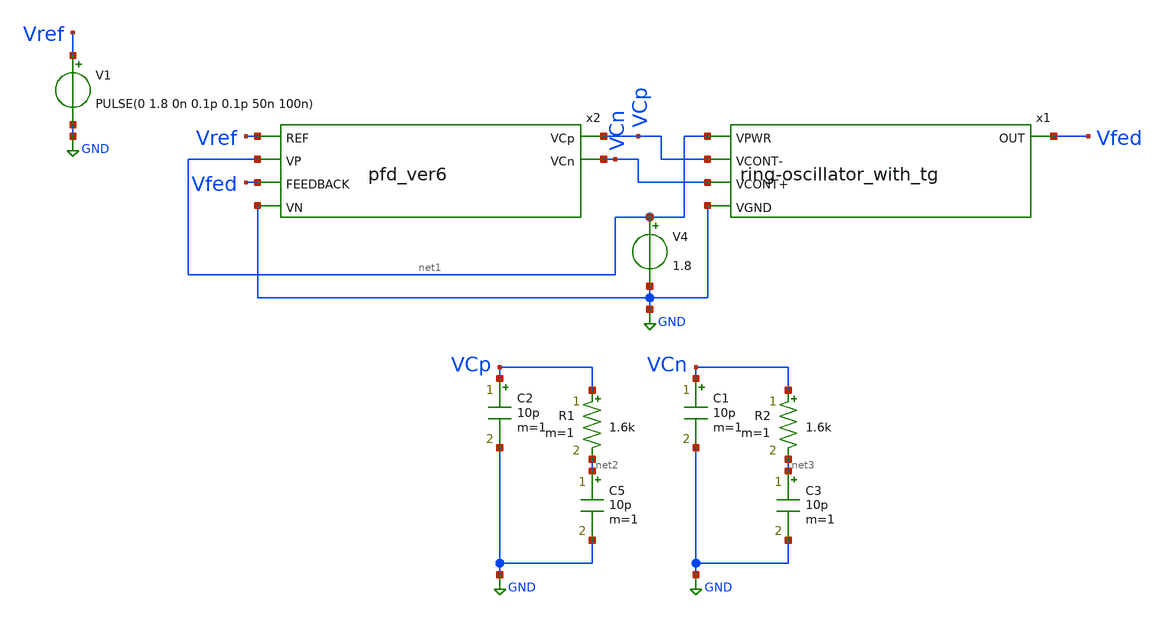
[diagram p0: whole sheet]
** sch_path: xschem_sch/pll_tb.sch
**.subckt pll_tb
V1 Vref GND PULSE(0 1.8 0n 0.1p 0.1p 50n 100n)
x1 net1 VCp Vfed VCn GND ring-oscillator_with_tg
V4 net1 GND 1.8
x2 Vref VCp VCn net1 Vfed GND pfd_ver6
C2 VCp GND 10p m=1
C5 net2 GND 10p m=1
R1 VCp net2 1.6k m=1
C1 VCn GND 10p m=1
C3 net3 GND 10p m=1
R2 VCn net3 1.6k m=1
**** begin user architecture code


.option wnflag=1
.option savecurrents
.control
save all
tran 1n 50u 0
plot VCp VCn
plot Vref Vfed
plot Vfed
.endc



** opencircuitdesign pdks install
.lib $::SKYWATER_MODELS/sky130.lib.spice tt
.param mc_mmm_cwitch=0
.param mc_pr_switch=1

**** end user architecture code
**.ends

* expanding   symbol:  ring-oscillator_with_tg.sym # of pins=5
** sym_path: xschem_sch/ring-oscillator_with_tg.sym
** sch_path: xschem_sch/ring-oscillator_with_tg.sch
.subckt ring-oscillator_with_tg VPWR VCONT- OUT VCONT+ VGND
*.ipin VPWR
*.opin OUT
*.ipin VGND
*.ipin VCONT+
*.ipin VCONT-
XM7 net1 net5 VPWR VPWR sky130_fd_pr__pfet_01v8 L=0.2 W=0.45 nf=1 ad='int((nf+1)/2) * W/nf * 0.29' as='int((nf+2)/2) * W/nf * 0.29'
+ pd='2*int((nf+1)/2) * (W/nf + 0.29)' ps='2*int((nf+2)/2) * (W/nf + 0.29)' nrd='0.29 / W' nrs='0.29 / W'
+ sa=0 sb=0 sd=0 mult=1 m=1
XM8 net3 VCONT- net1 VPWR sky130_fd_pr__pfet_01v8 L=0.2 W=0.45 nf=1 ad='int((nf+1)/2) * W/nf * 0.29'
+ as='int((nf+2)/2) * W/nf * 0.29' pd='2*int((nf+1)/2) * (W/nf + 0.29)' ps='2*int((nf+2)/2) * (W/nf + 0.29)'
+ nrd='0.29 / W' nrs='0.29 / W' sa=0 sb=0 sd=0 mult=1 m=1
XM9 net2 net3 VPWR VPWR sky130_fd_pr__pfet_01v8 L=0.2 W=0.45 nf=1 ad='int((nf+1)/2) * W/nf * 0.29' as='int((nf+2)/2) * W/nf * 0.29'
+ pd='2*int((nf+1)/2) * (W/nf + 0.29)' ps='2*int((nf+2)/2) * (W/nf + 0.29)' nrd='0.29 / W' nrs='0.29 / W'
+ sa=0 sb=0 sd=0 mult=1 m=1
XM11 OUT net4 VPWR VPWR sky130_fd_pr__pfet_01v8 L=0.2 W=0.45 nf=1 ad='int((nf+1)/2) * W/nf * 0.29' as='int((nf+2)/2) * W/nf * 0.29'
+ pd='2*int((nf+1)/2) * (W/nf + 0.29)' ps='2*int((nf+2)/2) * (W/nf + 0.29)' nrd='0.29 / W' nrs='0.29 / W'
+ sa=0 sb=0 sd=0 mult=1 m=1
XM10 net4 VCONT- net2 VPWR sky130_fd_pr__pfet_01v8 L=0.2 W=0.45 nf=1 ad='int((nf+1)/2) * W/nf * 0.29'
+ as='int((nf+2)/2) * W/nf * 0.29' pd='2*int((nf+1)/2) * (W/nf + 0.29)' ps='2*int((nf+2)/2) * (W/nf + 0.29)'
+ nrd='0.29 / W' nrs='0.29 / W' sa=0 sb=0 sd=0 mult=1 m=1
XM12 net5 VCONT- OUT VPWR sky130_fd_pr__pfet_01v8 L=0.2 W=0.45 nf=1 ad='int((nf+1)/2) * W/nf * 0.29'
+ as='int((nf+2)/2) * W/nf * 0.29' pd='2*int((nf+1)/2) * (W/nf + 0.29)' ps='2*int((nf+2)/2) * (W/nf + 0.29)'
+ nrd='0.29 / W' nrs='0.29 / W' sa=0 sb=0 sd=0 mult=1 m=1
XC1 VGND net5 sky130_fd_pr__cap_mim_m3_1 W=10 L=10 MF=1 m=1
XC2 VGND net3 sky130_fd_pr__cap_mim_m3_1 W=10 L=10 MF=1 m=1
XC3 VGND net4 sky130_fd_pr__cap_mim_m3_1 W=10 L=10 MF=10 m=10
XM13 OUT net4 VGND VGND sky130_fd_pr__nfet_01v8 L=0.2 W=0.45 nf=1 ad='int((nf+1)/2) * W/nf * 0.29' as='int((nf+2)/2) * W/nf * 0.29'
+ pd='2*int((nf+1)/2) * (W/nf + 0.29)' ps='2*int((nf+2)/2) * (W/nf + 0.29)' nrd='0.29 / W' nrs='0.29 / W'
+ sa=0 sb=0 sd=0 mult=1 m=1
XM1 net2 net3 VGND VGND sky130_fd_pr__nfet_01v8 L=0.2 W=0.45 nf=1 ad='int((nf+1)/2) * W/nf * 0.29' as='int((nf+2)/2) * W/nf * 0.29'
+ pd='2*int((nf+1)/2) * (W/nf + 0.29)' ps='2*int((nf+2)/2) * (W/nf + 0.29)' nrd='0.29 / W' nrs='0.29 / W'
+ sa=0 sb=0 sd=0 mult=1 m=1
XM2 net1 net5 VGND VGND sky130_fd_pr__nfet_01v8 L=0.2 W=0.45 nf=1 ad='int((nf+1)/2) * W/nf * 0.29' as='int((nf+2)/2) * W/nf * 0.29'
+ pd='2*int((nf+1)/2) * (W/nf + 0.29)' ps='2*int((nf+2)/2) * (W/nf + 0.29)' nrd='0.29 / W' nrs='0.29 / W'
+ sa=0 sb=0 sd=0 mult=1 m=1
XM3 OUT VCONT+ net5 VGND sky130_fd_pr__nfet_01v8 L=0.2 W=0.45 nf=1 ad='int((nf+1)/2) * W/nf * 0.29' as='int((nf+2)/2) * W/nf * 0.29'
+ pd='2*int((nf+1)/2) * (W/nf + 0.29)' ps='2*int((nf+2)/2) * (W/nf + 0.29)' nrd='0.29 / W' nrs='0.29 / W'
+ sa=0 sb=0 sd=0 mult=1 m=1
XM4 net1 VCONT+ net3 VGND sky130_fd_pr__nfet_01v8 L=0.2 W=0.45 nf=1 ad='int((nf+1)/2) * W/nf * 0.29'
+ as='int((nf+2)/2) * W/nf * 0.29' pd='2*int((nf+1)/2) * (W/nf + 0.29)' ps='2*int((nf+2)/2) * (W/nf + 0.29)'
+ nrd='0.29 / W' nrs='0.29 / W' sa=0 sb=0 sd=0 mult=1 m=1
XM5 net2 VCONT+ net4 VGND sky130_fd_pr__nfet_01v8 L=0.2 W=0.45 nf=1 ad='int((nf+1)/2) * W/nf * 0.29'
+ as='int((nf+2)/2) * W/nf * 0.29' pd='2*int((nf+1)/2) * (W/nf + 0.29)' ps='2*int((nf+2)/2) * (W/nf + 0.29)'
+ nrd='0.29 / W' nrs='0.29 / W' sa=0 sb=0 sd=0 mult=1 m=1
.ends


* expanding   symbol:  pfd_ver6.sym # of pins=6
** sym_path: xschem_sch/pfd_ver6.sym
** sch_path: xschem_sch/pfd_ver6.sch
.subckt pfd_ver6 REF VCp VCn VP FEEDBACK VN
*.opin VCn
*.ipin REF
*.ipin FEEDBACK
*.opin VCp
*.ipin VP
*.ipin VN
XM1 net1 REF VP VP sky130_fd_pr__pfet_01v8 L=0.15 W=0.45 nf=1 ad='int((nf+1)/2) * W/nf * 0.29' as='int((nf+2)/2) * W/nf * 0.29'
+ pd='2*int((nf+1)/2) * (W/nf + 0.29)' ps='2*int((nf+2)/2) * (W/nf + 0.29)' nrd='0.29 / W' nrs='0.29 / W'
+ sa=0 sb=0 sd=0 mult=1 m=1
XM2 net1 net2 VN VN sky130_fd_pr__nfet_01v8 L=0.15 W=0.45 nf=1 ad='int((nf+1)/2) * W/nf * 0.29' as='int((nf+2)/2) * W/nf * 0.29'
+ pd='2*int((nf+1)/2) * (W/nf + 0.29)' ps='2*int((nf+2)/2) * (W/nf + 0.29)' nrd='0.29 / W' nrs='0.29 / W'
+ sa=0 sb=0 sd=0 mult=1 m=1
XM3 net9 net1 VP VP sky130_fd_pr__pfet_01v8 L=0.15 W=0.45 nf=1 ad='int((nf+1)/2) * W/nf * 0.29' as='int((nf+2)/2) * W/nf * 0.29'
+ pd='2*int((nf+1)/2) * (W/nf + 0.29)' ps='2*int((nf+2)/2) * (W/nf + 0.29)' nrd='0.29 / W' nrs='0.29 / W'
+ sa=0 sb=0 sd=0 mult=1 m=1
XM4 net3 net9 VP VP sky130_fd_pr__pfet_01v8 L=0.15 W=0.45 nf=1 ad='int((nf+1)/2) * W/nf * 0.29' as='int((nf+2)/2) * W/nf * 0.29'
+ pd='2*int((nf+1)/2) * (W/nf + 0.29)' ps='2*int((nf+2)/2) * (W/nf + 0.29)' nrd='0.29 / W' nrs='0.29 / W'
+ sa=0 sb=0 sd=0 mult=1 m=1
XM5 net9 REF net8 VN sky130_fd_pr__nfet_01v8 L=0.15 W=0.45 nf=1 ad='int((nf+1)/2) * W/nf * 0.29' as='int((nf+2)/2) * W/nf * 0.29'
+ pd='2*int((nf+1)/2) * (W/nf + 0.29)' ps='2*int((nf+2)/2) * (W/nf + 0.29)' nrd='0.29 / W' nrs='0.29 / W'
+ sa=0 sb=0 sd=0 mult=1 m=1
XM6 net8 net1 VN VN sky130_fd_pr__nfet_01v8 L=0.15 W=0.45 nf=1 ad='int((nf+1)/2) * W/nf * 0.29' as='int((nf+2)/2) * W/nf * 0.29'
+ pd='2*int((nf+1)/2) * (W/nf + 0.29)' ps='2*int((nf+2)/2) * (W/nf + 0.29)' nrd='0.29 / W' nrs='0.29 / W'
+ sa=0 sb=0 sd=0 mult=1 m=1
XM7 net3 net9 VN VN sky130_fd_pr__nfet_01v8 L=0.15 W=0.45 nf=1 ad='int((nf+1)/2) * W/nf * 0.29' as='int((nf+2)/2) * W/nf * 0.29'
+ pd='2*int((nf+1)/2) * (W/nf + 0.29)' ps='2*int((nf+2)/2) * (W/nf + 0.29)' nrd='0.29 / W' nrs='0.29 / W'
+ sa=0 sb=0 sd=0 mult=1 m=1
XM8 net2 net4 net3 VP sky130_fd_pr__pfet_01v8 L=0.15 W=0.45 nf=1 ad='int((nf+1)/2) * W/nf * 0.29' as='int((nf+2)/2) * W/nf * 0.29'
+ pd='2*int((nf+1)/2) * (W/nf + 0.29)' ps='2*int((nf+2)/2) * (W/nf + 0.29)' nrd='0.29 / W' nrs='0.29 / W'
+ sa=0 sb=0 sd=0 mult=1 m=1
XM9 net2 net4 VN VN sky130_fd_pr__nfet_01v8 L=0.15 W=0.45 nf=1 ad='int((nf+1)/2) * W/nf * 0.29' as='int((nf+2)/2) * W/nf * 0.29'
+ pd='2*int((nf+1)/2) * (W/nf + 0.29)' ps='2*int((nf+2)/2) * (W/nf + 0.29)' nrd='0.29 / W' nrs='0.29 / W'
+ sa=0 sb=0 sd=0 mult=1 m=1
XM10 net5 net4 VP VP sky130_fd_pr__pfet_01v8 L=0.15 W=0.45 nf=1 ad='int((nf+1)/2) * W/nf * 0.29' as='int((nf+2)/2) * W/nf * 0.29'
+ pd='2*int((nf+1)/2) * (W/nf + 0.29)' ps='2*int((nf+2)/2) * (W/nf + 0.29)' nrd='0.29 / W' nrs='0.29 / W'
+ sa=0 sb=0 sd=0 mult=1 m=1
XM11 net5 net4 VN VN sky130_fd_pr__nfet_01v8 L=0.15 W=0.45 nf=1 ad='int((nf+1)/2) * W/nf * 0.29' as='int((nf+2)/2) * W/nf * 0.29'
+ pd='2*int((nf+1)/2) * (W/nf + 0.29)' ps='2*int((nf+2)/2) * (W/nf + 0.29)' nrd='0.29 / W' nrs='0.29 / W'
+ sa=0 sb=0 sd=0 mult=1 m=1
XM12 net4 net7 VP VP sky130_fd_pr__pfet_01v8 L=0.15 W=0.45 nf=1 ad='int((nf+1)/2) * W/nf * 0.29' as='int((nf+2)/2) * W/nf * 0.29'
+ pd='2*int((nf+1)/2) * (W/nf + 0.29)' ps='2*int((nf+2)/2) * (W/nf + 0.29)' nrd='0.29 / W' nrs='0.29 / W'
+ sa=0 sb=0 sd=0 mult=1 m=1
XM13 net4 FEEDBACK net6 VN sky130_fd_pr__nfet_01v8 L=0.15 W=0.45 nf=1 ad='int((nf+1)/2) * W/nf * 0.29'
+ as='int((nf+2)/2) * W/nf * 0.29' pd='2*int((nf+1)/2) * (W/nf + 0.29)' ps='2*int((nf+2)/2) * (W/nf + 0.29)'
+ nrd='0.29 / W' nrs='0.29 / W' sa=0 sb=0 sd=0 mult=1 m=1
XM14 net7 FEEDBACK VP VP sky130_fd_pr__pfet_01v8 L=0.15 W=0.45 nf=1 ad='int((nf+1)/2) * W/nf * 0.29'
+ as='int((nf+2)/2) * W/nf * 0.29' pd='2*int((nf+1)/2) * (W/nf + 0.29)' ps='2*int((nf+2)/2) * (W/nf + 0.29)'
+ nrd='0.29 / W' nrs='0.29 / W' sa=0 sb=0 sd=0 mult=1 m=1
XM15 net7 net2 VN VN sky130_fd_pr__nfet_01v8 L=0.15 W=0.45 nf=1 ad='int((nf+1)/2) * W/nf * 0.29' as='int((nf+2)/2) * W/nf * 0.29'
+ pd='2*int((nf+1)/2) * (W/nf + 0.29)' ps='2*int((nf+2)/2) * (W/nf + 0.29)' nrd='0.29 / W' nrs='0.29 / W'
+ sa=0 sb=0 sd=0 mult=1 m=1
XM16 net6 net7 VN VN sky130_fd_pr__nfet_01v8 L=0.15 W=0.45 nf=1 ad='int((nf+1)/2) * W/nf * 0.29' as='int((nf+2)/2) * W/nf * 0.29'
+ pd='2*int((nf+1)/2) * (W/nf + 0.29)' ps='2*int((nf+2)/2) * (W/nf + 0.29)' nrd='0.29 / W' nrs='0.29 / W'
+ sa=0 sb=0 sd=0 mult=1 m=1
XM45 VCp net5 VN VN sky130_fd_pr__nfet_01v8 L=0.15 W=0.45 nf=1 ad='int((nf+1)/2) * W/nf * 0.29' as='int((nf+2)/2) * W/nf * 0.29'
+ pd='2*int((nf+1)/2) * (W/nf + 0.29)' ps='2*int((nf+2)/2) * (W/nf + 0.29)' nrd='0.29 / W' nrs='0.29 / W'
+ sa=0 sb=0 sd=0 mult=1 m=1
XM44 VCp net11 VP VP sky130_fd_pr__pfet_01v8 L=0.15 W=0.45 nf=1 ad='int((nf+1)/2) * W/nf * 0.29' as='int((nf+2)/2) * W/nf * 0.29'
+ pd='2*int((nf+1)/2) * (W/nf + 0.29)' ps='2*int((nf+2)/2) * (W/nf + 0.29)' nrd='0.29 / W' nrs='0.29 / W'
+ sa=0 sb=0 sd=0 mult=1 m=1
XM17 VCn net3 VP VP sky130_fd_pr__pfet_01v8 L=0.15 W=0.45 nf=1 ad='int((nf+1)/2) * W/nf * 0.29' as='int((nf+2)/2) * W/nf * 0.29'
+ pd='2*int((nf+1)/2) * (W/nf + 0.29)' ps='2*int((nf+2)/2) * (W/nf + 0.29)' nrd='0.29 / W' nrs='0.29 / W'
+ sa=0 sb=0 sd=0 mult=1 m=1
XM18 VCn net10 VN VN sky130_fd_pr__nfet_01v8 L=0.15 W=0.45 nf=1 ad='int((nf+1)/2) * W/nf * 0.29' as='int((nf+2)/2) * W/nf * 0.29'
+ pd='2*int((nf+1)/2) * (W/nf + 0.29)' ps='2*int((nf+2)/2) * (W/nf + 0.29)' nrd='0.29 / W' nrs='0.29 / W'
+ sa=0 sb=0 sd=0 mult=1 m=1
XM19 net11 VN net9 VP sky130_fd_pr__pfet_01v8 L=0.15 W=0.45 nf=1 ad='int((nf+1)/2) * W/nf * 0.29' as='int((nf+2)/2) * W/nf * 0.29'
+ pd='2*int((nf+1)/2) * (W/nf + 0.29)' ps='2*int((nf+2)/2) * (W/nf + 0.29)' nrd='0.29 / W' nrs='0.29 / W'
+ sa=0 sb=0 sd=0 mult=1 m=1
XM20 net9 VP net11 VN sky130_fd_pr__nfet_01v8 L=0.15 W=0.45 nf=1 ad='int((nf+1)/2) * W/nf * 0.29' as='int((nf+2)/2) * W/nf * 0.29'
+ pd='2*int((nf+1)/2) * (W/nf + 0.29)' ps='2*int((nf+2)/2) * (W/nf + 0.29)' nrd='0.29 / W' nrs='0.29 / W'
+ sa=0 sb=0 sd=0 mult=1 m=1
XM21 net10 VN net4 VP sky130_fd_pr__pfet_01v8 L=0.15 W=0.45 nf=1 ad='int((nf+1)/2) * W/nf * 0.29' as='int((nf+2)/2) * W/nf * 0.29'
+ pd='2*int((nf+1)/2) * (W/nf + 0.29)' ps='2*int((nf+2)/2) * (W/nf + 0.29)' nrd='0.29 / W' nrs='0.29 / W'
+ sa=0 sb=0 sd=0 mult=1 m=1
XM22 net4 VP net10 VN sky130_fd_pr__nfet_01v8 L=0.15 W=0.45 nf=1 ad='int((nf+1)/2) * W/nf * 0.29' as='int((nf+2)/2) * W/nf * 0.29'
+ pd='2*int((nf+1)/2) * (W/nf + 0.29)' ps='2*int((nf+2)/2) * (W/nf + 0.29)' nrd='0.29 / W' nrs='0.29 / W'
+ sa=0 sb=0 sd=0 mult=1 m=1
.ends

.GLOBAL GND
.end
